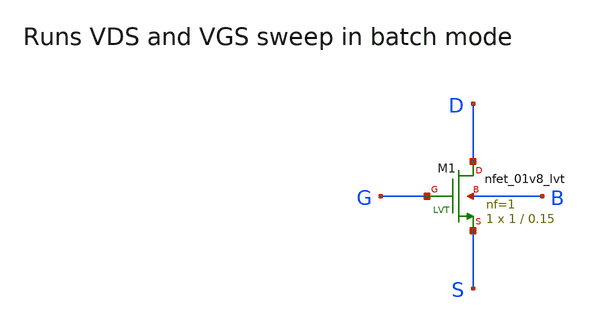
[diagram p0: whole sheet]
** sch_path: nmos_tb.sch
**.subckt nmos_tb
XM1 D G S B sky130_fd_pr__nfet_01v8_lvt L=0.15 W=1 nf=1 ad='int((nf+1)/2) * W/nf * 0.29' as='int((nf+2)/2) * W/nf * 0.29'
+ pd='2*int((nf+1)/2) * (W/nf + 0.29)' ps='2*int((nf+2)/2) * (W/nf + 0.29)' nrd='0.29 / W' nrs='0.29 / W'
+ sa=0 sb=0 sd=0 mult=1 m=1
**** begin user architecture code


Vg G 0 1.8
Vs S 0 0
Vd D 0 1.8
Vb B 0 0

.dc Vd 0 1.8 0.1 Vg 0 1.8 0.6
.save v(G) v(D) v(S) v(B)
.save @m.xm1.msky130_fd_pr__nfet_01v8_lvt[gm]
.save @m.xm1.msky130_fd_pr__nfet_01v8_lvt[gmbs]
.save @m.xm1.msky130_fd_pr__nfet_01v8_lvt[gds]
.save @m.xm1.msky130_fd_pr__nfet_01v8_lvt[vdsat]
.save @m.xm1.msky130_fd_pr__nfet_01v8_lvt[vth]
.save @m.xm1.msky130_fd_pr__nfet_01v8_lvt[id]
.save @m.xm1.msky130_fd_pr__nfet_01v8_lvt[vbs]
.save @m.xm1.msky130_fd_pr__nfet_01v8_lvt[vgs]
.save @m.xm1.msky130_fd_pr__nfet_01v8_lvt[vds]
.save @m.xm1.msky130_fd_pr__nfet_01v8_lvt[cgg]
.save @m.xm1.msky130_fd_pr__nfet_01v8_lvt[cgs]
.save @m.xm1.msky130_fd_pr__nfet_01v8_lvt[cgd]
.save @m.xm1.msky130_fd_pr__nfet_01v8_lvt[cbg]
.save @m.xm1.msky130_fd_pr__nfet_01v8_lvt[cbd]
.save @m.xm1.msky130_fd_pr__nfet_01v8_lvt[cbs]
.save @m.xm1.msky130_fd_pr__nfet_01v8_lvt[cdg]
.save @m.xm1.msky130_fd_pr__nfet_01v8_lvt[cdd]
.save @m.xm1.msky130_fd_pr__nfet_01v8_lvt[cds]
.save @m.xm1.msky130_fd_pr__nfet_01v8_lvt[csg]
.save @m.xm1.msky130_fd_pr__nfet_01v8_lvt[csd]
.save @m.xm1.msky130_fd_pr__nfet_01v8_lvt[css]
.save @m.xm1.msky130_fd_pr__nfet_01v8_lvt[cgb]
.save @m.xm1.msky130_fd_pr__nfet_01v8_lvt[cdb]
.save @m.xm1.msky130_fd_pr__nfet_01v8_lvt[csb]
.save @m.xm1.msky130_fd_pr__nfet_01v8_lvt[cbb]
.save @m.xm1.msky130_fd_pr__nfet_01v8_lvt[capbd]
.save @m.xm1.msky130_fd_pr__nfet_01v8_lvt[capbs]


*.control
*save all
*dc Vd 0 1.8 0.05 Vg 0 1.8 0.3
*plot all.vd1#branch vs D1v8
*plot all.vd2#branch vs D1v8
*plot all.vd3#branch vs D3v3
*plot all.vd4#branch vs D5v0
*plot all.vd5#branch vs D10v5
*plot all.vd6#branch vs D16v0
*plot all.vd8#branch vs D1v8
*plot all.vd7#branch vs D1v8
*save @m.xm1.msky130_fd_pr__nfet_01v8_lvt[gm]
*op
*write test_nmos.raw
*.endc



.include $::SKYWATER_MODELS/cells/nfet_01v8/sky130_fd_pr__nfet_01v8__tt.corner.spice
.include $::SKYWATER_MODELS/cells/nfet_01v8_lvt/sky130_fd_pr__nfet_01v8_lvt__tt.corner.spice
.include $::SKYWATER_MODELS/cells/pfet_01v8/sky130_fd_pr__pfet_01v8__tt.corner.spice
.include $::SKYWATER_MODELS/cells/nfet_03v3_nvt/sky130_fd_pr__nfet_03v3_nvt__tt.corner.spice
.include $::SKYWATER_MODELS/cells/nfet_05v0_nvt/sky130_fd_pr__nfet_05v0_nvt__tt.corner.spice
.include $::SKYWATER_MODELS/cells/esd_nfet_01v8/sky130_fd_pr__esd_nfet_01v8__tt.corner.spice
.include $::SKYWATER_MODELS/cells/pfet_01v8_lvt/sky130_fd_pr__pfet_01v8_lvt__tt.corner.spice
.include $::SKYWATER_MODELS/cells/pfet_01v8_hvt/sky130_fd_pr__pfet_01v8_hvt__tt.corner.spice
.include $::SKYWATER_MODELS/cells/esd_pfet_g5v0d10v5/sky130_fd_pr__esd_pfet_g5v0d10v5__tt.corner.spice
.include $::SKYWATER_MODELS/cells/pfet_g5v0d10v5/sky130_fd_pr__pfet_g5v0d10v5__tt.corner.spice
.include $::SKYWATER_MODELS/cells/pfet_g5v0d16v0/sky130_fd_pr__pfet_g5v0d16v0__tt.corner.spice
.include $::SKYWATER_MODELS/cells/nfet_g5v0d10v5/sky130_fd_pr__nfet_g5v0d10v5__tt.corner.spice
.include $::SKYWATER_MODELS/cells/nfet_g5v0d16v0/sky130_fd_pr__nfet_g5v0d16v0__tt_discrete.corner.spice
.include $::SKYWATER_MODELS/cells/esd_nfet_g5v0d10v5/sky130_fd_pr__esd_nfet_g5v0d10v5__tt.corner.spice
.include $::SKYWATER_MODELS/models/corners/tt/nonfet.spice
* Mismatch parameters
.include $::SKYWATER_MODELS/cells/nfet_01v8/sky130_fd_pr__nfet_01v8__mismatch.corner.spice
.include $::SKYWATER_MODELS/cells/pfet_01v8/sky130_fd_pr__pfet_01v8__mismatch.corner.spice
.include $::SKYWATER_MODELS/cells/nfet_01v8_lvt/sky130_fd_pr__nfet_01v8_lvt__mismatch.corner.spice
.include $::SKYWATER_MODELS/cells/pfet_01v8_lvt/sky130_fd_pr__pfet_01v8_lvt__mismatch.corner.spice
.include $::SKYWATER_MODELS/cells/pfet_01v8_hvt/sky130_fd_pr__pfet_01v8_hvt__mismatch.corner.spice
.include $::SKYWATER_MODELS/cells/nfet_g5v0d10v5/sky130_fd_pr__nfet_g5v0d10v5__mismatch.corner.spice
.include $::SKYWATER_MODELS/cells/pfet_g5v0d10v5/sky130_fd_pr__pfet_g5v0d10v5__mismatch.corner.spice
.include $::SKYWATER_MODELS/cells/nfet_05v0_nvt/sky130_fd_pr__nfet_05v0_nvt__mismatch.corner.spice
.include $::SKYWATER_MODELS/cells/nfet_03v3_nvt/sky130_fd_pr__nfet_03v3_nvt__mismatch.corner.spice
* Resistor$::SKYWATER_MODELS/Capacitor
.include $::SKYWATER_MODELS/models/r+c/res_typical__cap_typical.spice
.include $::SKYWATER_MODELS/models/r+c/res_typical__cap_typical__lin.spice
* Special cells
.include $::SKYWATER_MODELS/models/corners/tt/specialized_cells.spice
* All models
.include $::SKYWATER_MODELS/models/all.spice
* Corner
.include $::SKYWATER_MODELS/models/corners/tt/rf.spice

**** end user architecture code
**.ends
.end
